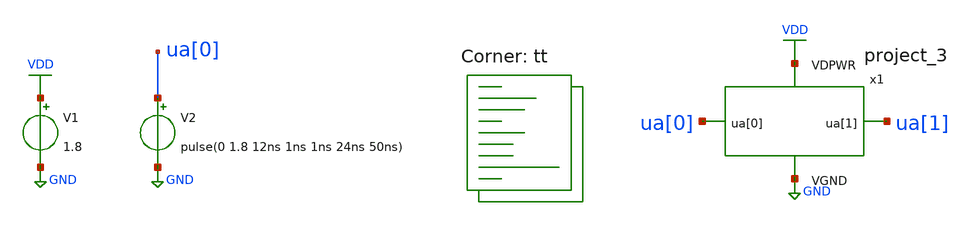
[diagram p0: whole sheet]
** sch_path: mag/tb_project_magic.sch
**.subckt tb_project_magic
V1 VDD GND 1.8
V2 ua[0] GND pulse(0 1.8 12ns 1ns 1ns 24ns 50ns)
x1 ua[1] VDD GND ua[0] project_3
**** begin user architecture code
.lib $::SKYWATER_MODELS/sky130.lib.spice tt



* .include /foss/designs/TTSKY25a-PLL/mag/project_magic.spice
.include /foss/designs/TTSKY25a-PLL/mag/project_3.spice

.option method=gear
* .option method=trap
.option wnflag=1
* .option savecurrents
* .options RSHUNT=1e15
* .options RSHUNT

.save v(ua[0]) v(ua[1]) v(x1.v_cont.n0) v(x1.v_cont.t0) v(x1.ua[0].n0) v(x1.ua[0].t0) v(x1.ua[1].n0) v(x1.ua[1].t0) @m.x1.x12.msky130_fd_pr__pfet_01v8[id] @m.x1.x47.msky130_fd_pr__pfet_01v8[id] @m.x1.x93.msky130_fd_pr__pfet_01v8[id] @m.x1.x110.msky130_fd_pr__pfet_01v8[id] @m.x1.x220.msky130_fd_pr__pfet_01v8[id] @m.x1.x252.msky130_fd_pr__pfet_01v8[id] @m.x1.x296.msky130_fd_pr__pfet_01v8[id] @m.x1.x343.msky130_fd_pr__pfet_01v8[id] @m.x1.x364.msky130_fd_pr__pfet_01v8[id] @m.x1.x428.msky130_fd_pr__pfet_01v8[id]

* V_out initial voltage

.ic v(x1.v_cont.n0) = 0.0


.control
  * save v(v_osc)

  * timestep for exact simulation results
  tran 5ps 5us


  remzerovec
  * write tb_project_magic_2.raw
  * write tb_project_magic_3.raw
  * write tb_project_magic_4.raw
  * write tb_project_magic_5.raw
  * write tb_project_magic_6.raw
  * write tb_project_magic_7.raw
  * write tb_project_magic_8.raw
  * write tb_project_magic_9.raw
  * write tb_project_magic_10.raw
  * write tb_project_magic_11.raw
  * write tb_project_magic_12.raw
  * write tb_project_magic_13.raw
  * write tb_project_magic_14.raw
  * write tb_project_magic_15.raw
  * write tb_project_magic_16.raw
  * write tb_project_magic_17.raw
  * write tb_project_magic_18.raw
  write tb_project_magic_19.raw
  wrdata /foss/designs/TTSKY25a-PLL/mag/tb_project_magic_v_osc.txt v(x1.ua[1].n0)

  set appendwrite

.endc



**** end user architecture code
**.ends
.GLOBAL GND
.GLOBAL VDD
.end
